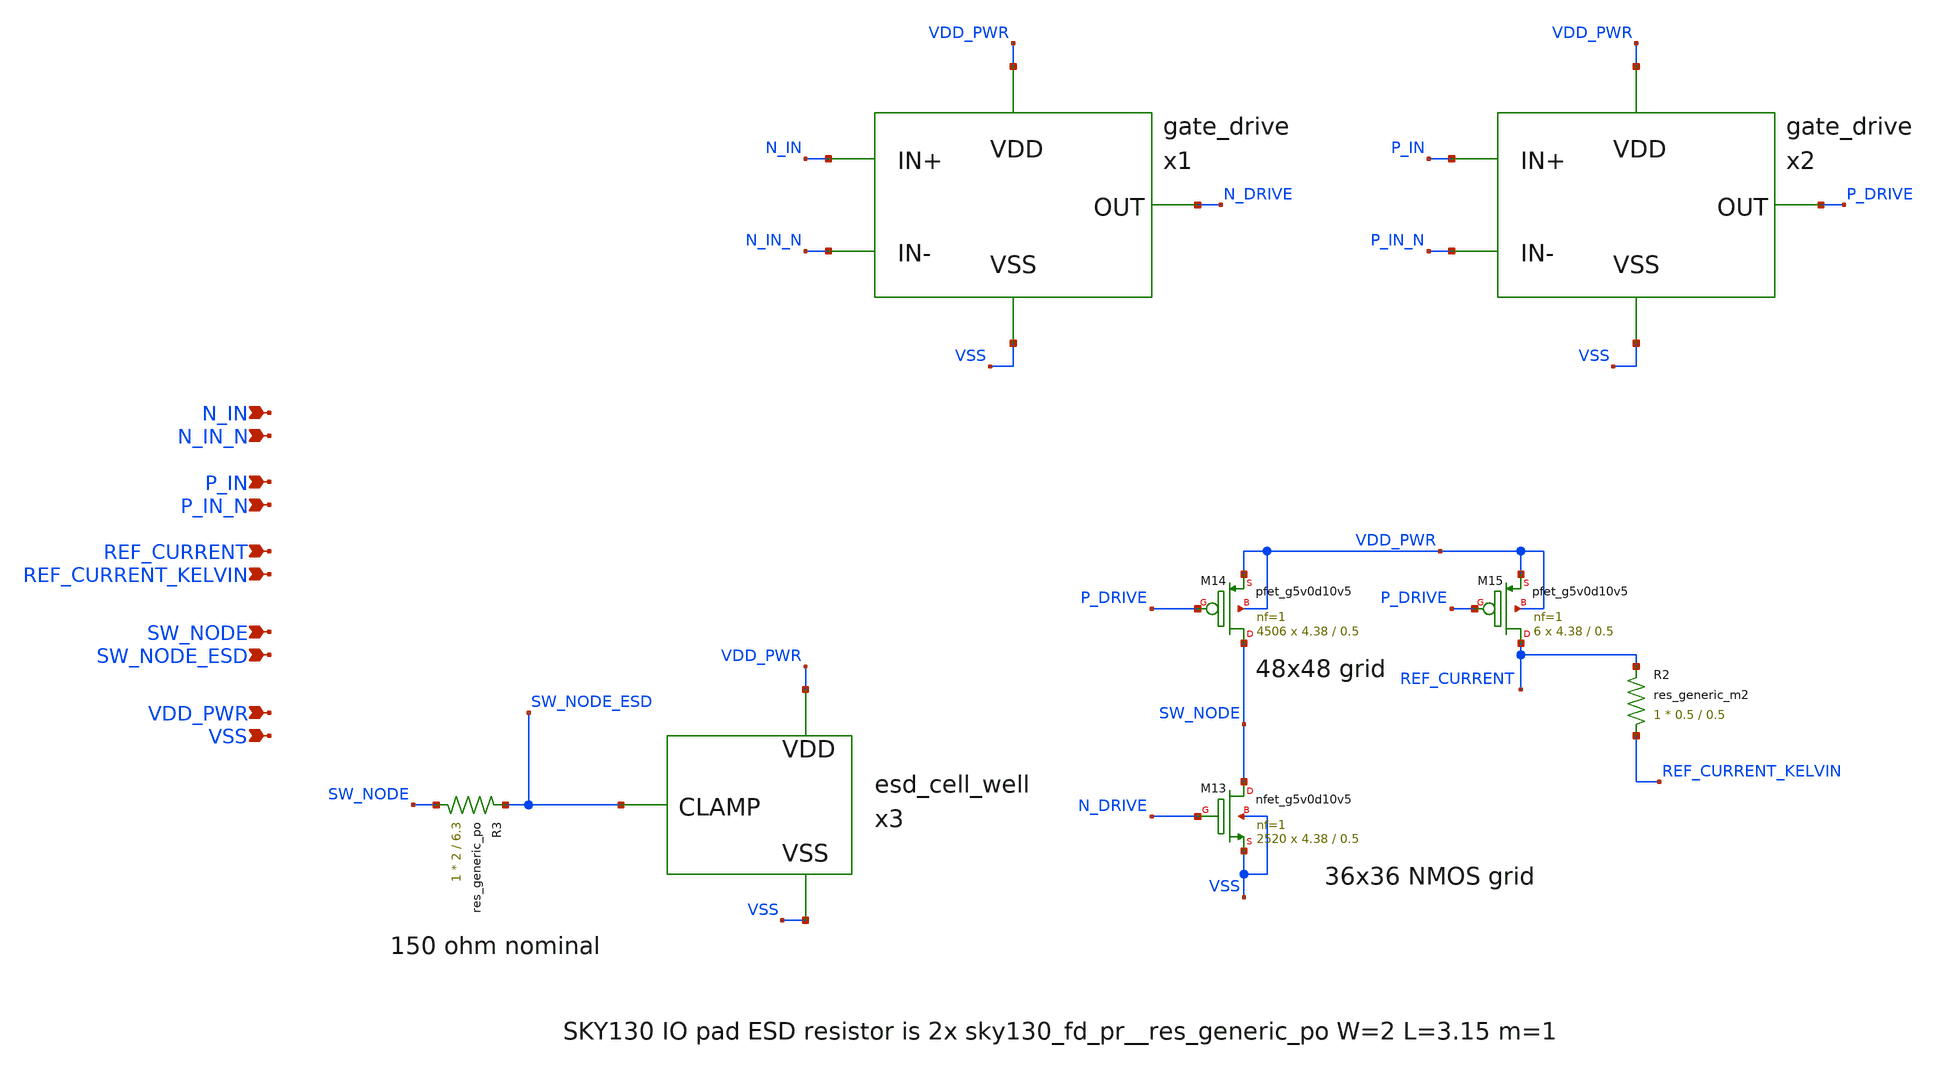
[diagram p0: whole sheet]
** sch_path: images/foss-asic-tools/addons/examples/Open-PMIC-tapeout/xschem/power_stage.sch
**.subckt power_stage N_IN N_IN_N P_IN P_IN_N REF_CURRENT REF_CURRENT_KELVIN SW_NODE SW_NODE_ESD
*+ VDD_PWR VSS
*.ipin N_IN
*.ipin N_IN_N
*.ipin P_IN
*.ipin P_IN_N
*.ipin REF_CURRENT
*.ipin REF_CURRENT_KELVIN
*.ipin SW_NODE
*.ipin SW_NODE_ESD
*.ipin VDD_PWR
*.ipin VSS
XM14 SW_NODE P_DRIVE VDD_PWR VDD_PWR sky130_fd_pr__pfet_g5v0d10v5 L=0.5 W=4.38 nf=1 ad='int((nf+1)/2) * W/nf * 0.29'
+ as='int((nf+2)/2) * W/nf * 0.29' pd='2*int((nf+1)/2) * (W/nf + 0.29)' ps='2*int((nf+2)/2) * (W/nf + 0.29)'
+ nrd='0.29 / W' nrs='0.29 / W' sa=0 sb=0 sd=0 mult=4506 m=4506
XM15 REF_CURRENT P_DRIVE VDD_PWR VDD_PWR sky130_fd_pr__pfet_g5v0d10v5 L=0.5 W=4.38 nf=1 ad='int((nf+1)/2) * W/nf * 0.29'
+ as='int((nf+2)/2) * W/nf * 0.29' pd='2*int((nf+1)/2) * (W/nf + 0.29)' ps='2*int((nf+2)/2) * (W/nf + 0.29)'
+ nrd='0.29 / W' nrs='0.29 / W' sa=0 sb=0 sd=0 mult=6 m=6
XM13 SW_NODE N_DRIVE VSS VSS sky130_fd_pr__nfet_g5v0d10v5 L=0.5 W=4.38 nf=1 ad='int((nf+1)/2) * W/nf * 0.29'
+ as='int((nf+2)/2) * W/nf * 0.29' pd='2*int((nf+1)/2) * (W/nf + 0.29)' ps='2*int((nf+2)/2) * (W/nf + 0.29)'
+ nrd='0.29 / W' nrs='0.29 / W' sa=0 sb=0 sd=0 mult=2520 m=2520
x1 N_IN N_IN_N VDD_PWR VSS N_DRIVE gate_drive
x2 P_IN P_IN_N VDD_PWR VSS P_DRIVE gate_drive
RR2 REF_CURRENT_KELVIN REF_CURRENT sky130_fd_pr__res_generic_m2 W=0.5 L=0.5 m=1
x3 VDD_PWR VSS SW_NODE_ESD esd_cell_well
RR3 SW_NODE SW_NODE_ESD sky130_fd_pr__res_generic_po W=2 L=6.3 m=1
**.ends
.end
